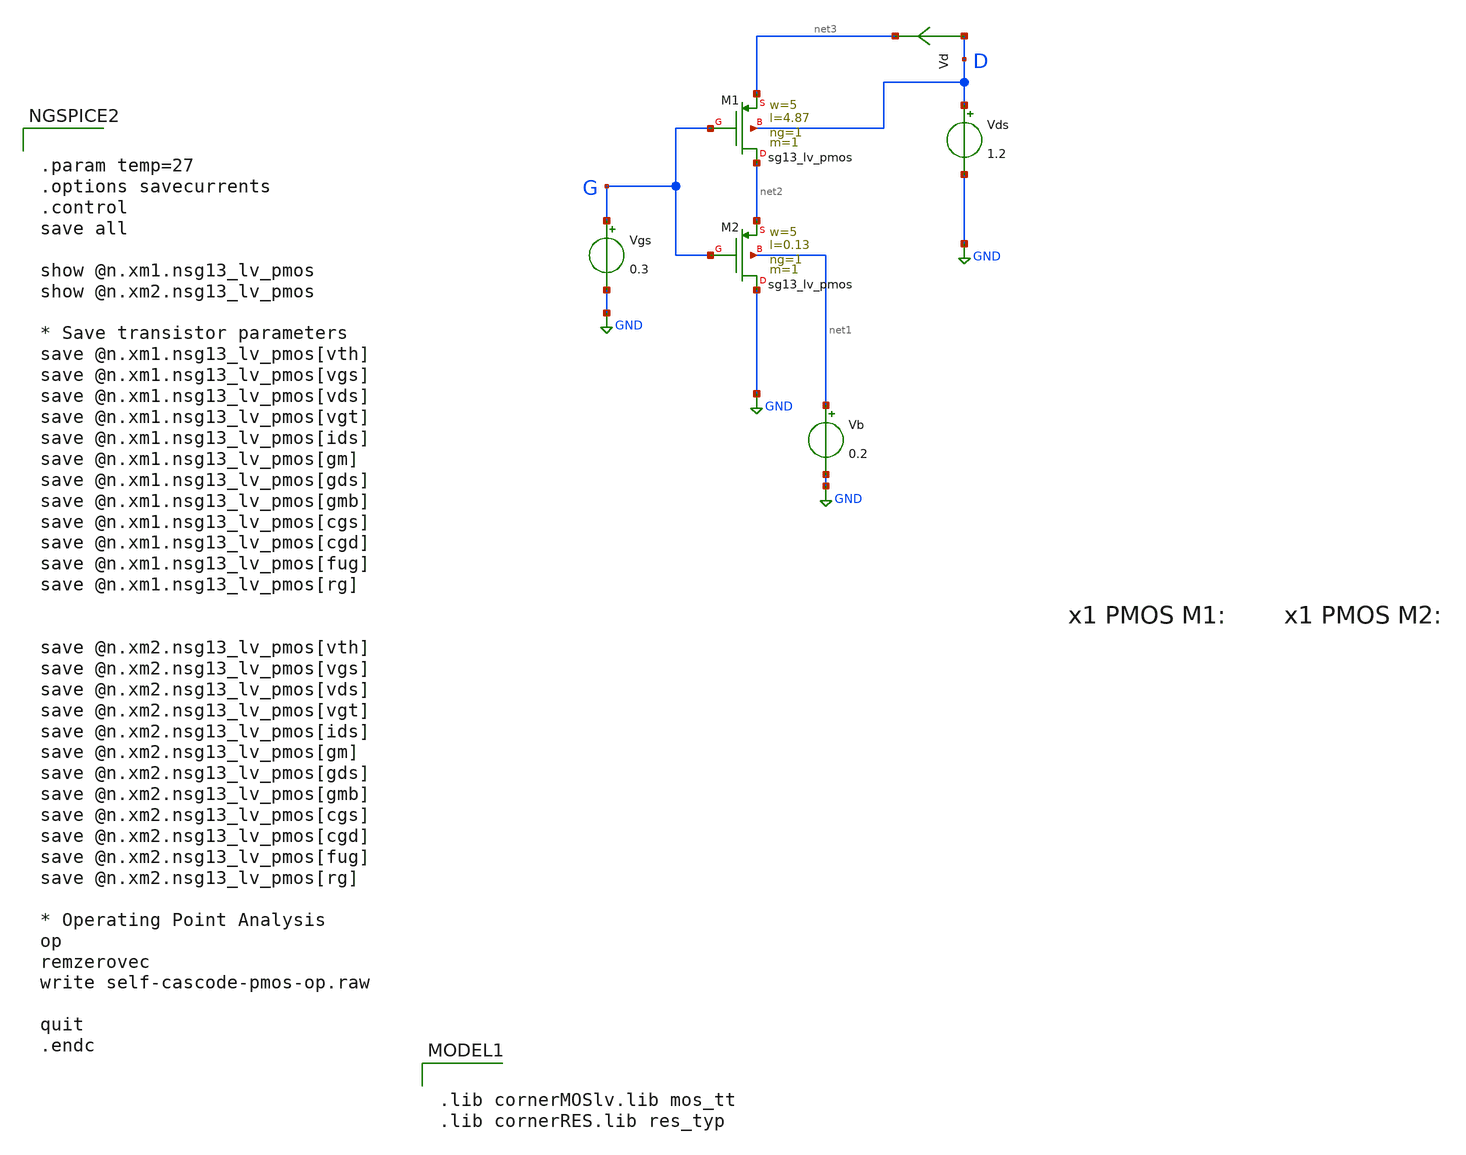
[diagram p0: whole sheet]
** sch_path: xschem/self-cascode-pmos-op.sch
**.subckt self-cascode-pmos-op
Vgs G GND 0.3
Vds D GND 1.2
Vd D net3 0
.save i(vd)
Vb net1 GND 0.2
XM1 net2 G net3 D sg13_lv_pmos w=5 l=4.87 ng=1 m=1 mm_ok=1
XM2 GND net4 net2 net1 sg13_lv_pmos w=5 l=0.13 ng=1 m=1 mm_ok=1
**** begin user architecture code

.lib cornerMOSlv.lib mos_tt
.lib cornerRES.lib res_typ



.param temp=27
.options savecurrents
.control
save all

show @n.xm1.nsg13_lv_pmos
show @n.xm2.nsg13_lv_pmos

* Save transistor parameters
save @n.xm1.nsg13_lv_pmos[vth]
save @n.xm1.nsg13_lv_pmos[vgs]
save @n.xm1.nsg13_lv_pmos[vds]
save @n.xm1.nsg13_lv_pmos[vgt]
save @n.xm1.nsg13_lv_pmos[ids]
save @n.xm1.nsg13_lv_pmos[gm]
save @n.xm1.nsg13_lv_pmos[gds]
save @n.xm1.nsg13_lv_pmos[gmb]
save @n.xm1.nsg13_lv_pmos[cgs]
save @n.xm1.nsg13_lv_pmos[cgd]
save @n.xm1.nsg13_lv_pmos[fug]
save @n.xm1.nsg13_lv_pmos[rg]


save @n.xm2.nsg13_lv_pmos[vth]
save @n.xm2.nsg13_lv_pmos[vgs]
save @n.xm2.nsg13_lv_pmos[vds]
save @n.xm2.nsg13_lv_pmos[vgt]
save @n.xm2.nsg13_lv_pmos[ids]
save @n.xm2.nsg13_lv_pmos[gm]
save @n.xm2.nsg13_lv_pmos[gds]
save @n.xm2.nsg13_lv_pmos[gmb]
save @n.xm2.nsg13_lv_pmos[cgs]
save @n.xm2.nsg13_lv_pmos[cgd]
save @n.xm2.nsg13_lv_pmos[fug]
save @n.xm2.nsg13_lv_pmos[rg]

* Operating Point Analysis
op
remzerovec
write self-cascode-pmos-op.raw

quit
.endc

**** end user architecture code
**.ends
.GLOBAL GND
.end
